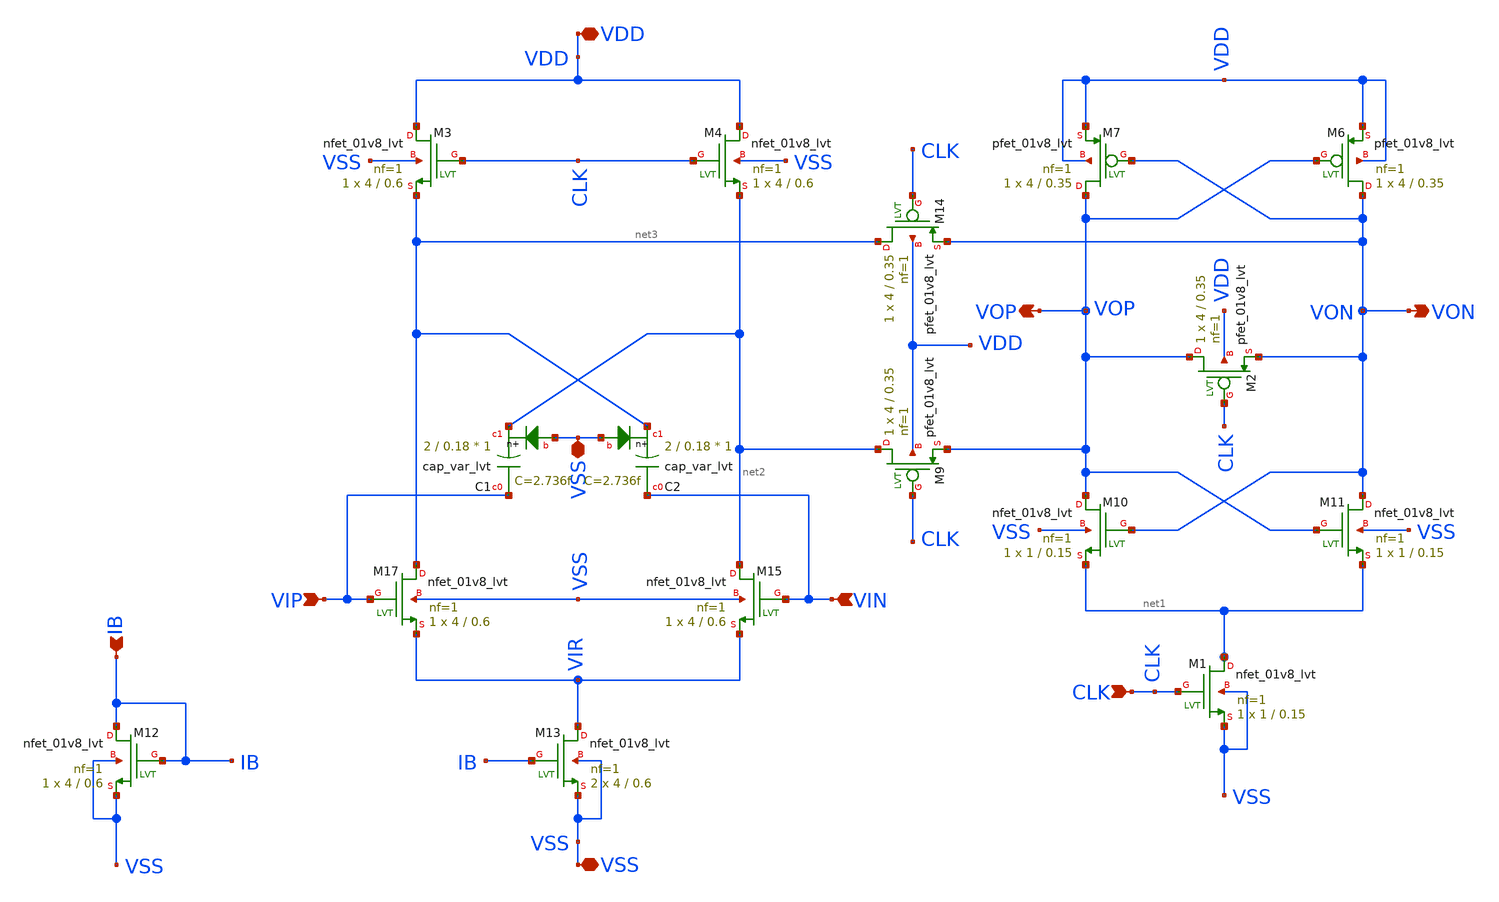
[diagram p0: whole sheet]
** sch_path: strongARM/class_AB_v3_sym.sch
**.subckt class_AB_v3_sym VDD IB VSS VIP VIN VON VOP CLK VSS
*.iopin VDD
*.ipin IB
*.iopin VSS
*.ipin VIP
*.ipin VIN
*.opin VON
*.opin VOP
*.ipin CLK
*.iopin VSS
XM17 net3 VIP VIR VSS sky130_fd_pr__nfet_01v8_lvt L=0.6 W=4 nf=1 ad='int((nf+1)/2) * W/nf * 0.29' as='int((nf+2)/2) * W/nf * 0.29'
+ pd='2*int((nf+1)/2) * (W/nf + 0.29)' ps='2*int((nf+2)/2) * (W/nf + 0.29)' nrd='0.29 / W' nrs='0.29 / W'
+ sa=0 sb=0 sd=0 mult=1 m=1
XM12 IB IB VSS VSS sky130_fd_pr__nfet_01v8_lvt L=0.6 W=4 nf=1 ad='int((nf+1)/2) * W/nf * 0.29' as='int((nf+2)/2) * W/nf * 0.29'
+ pd='2*int((nf+1)/2) * (W/nf + 0.29)' ps='2*int((nf+2)/2) * (W/nf + 0.29)' nrd='0.29 / W' nrs='0.29 / W'
+ sa=0 sb=0 sd=0 mult=1 m=1
XM15 net2 VIN VIR VSS sky130_fd_pr__nfet_01v8_lvt L=0.6 W=4 nf=1 ad='int((nf+1)/2) * W/nf * 0.29' as='int((nf+2)/2) * W/nf * 0.29'
+ pd='2*int((nf+1)/2) * (W/nf + 0.29)' ps='2*int((nf+2)/2) * (W/nf + 0.29)' nrd='0.29 / W' nrs='0.29 / W'
+ sa=0 sb=0 sd=0 mult=1 m=1
XM13 VIR IB VSS VSS sky130_fd_pr__nfet_01v8_lvt L=0.6 W=4 nf=1 ad='int((nf+1)/2) * W/nf * 0.29' as='int((nf+2)/2) * W/nf * 0.29'
+ pd='2*int((nf+1)/2) * (W/nf + 0.29)' ps='2*int((nf+2)/2) * (W/nf + 0.29)' nrd='0.29 / W' nrs='0.29 / W'
+ sa=0 sb=0 sd=0 mult=2 m=2
XM6 VON VOP VDD VDD sky130_fd_pr__pfet_01v8_lvt L=0.35 W=4 nf=1 ad='int((nf+1)/2) * W/nf * 0.29' as='int((nf+2)/2) * W/nf * 0.29'
+ pd='2*int((nf+1)/2) * (W/nf + 0.29)' ps='2*int((nf+2)/2) * (W/nf + 0.29)' nrd='0.29 / W' nrs='0.29 / W'
+ sa=0 sb=0 sd=0 mult=1 m=1
XM7 VOP VON VDD VDD sky130_fd_pr__pfet_01v8_lvt L=0.35 W=4 nf=1 ad='int((nf+1)/2) * W/nf * 0.29' as='int((nf+2)/2) * W/nf * 0.29'
+ pd='2*int((nf+1)/2) * (W/nf + 0.29)' ps='2*int((nf+2)/2) * (W/nf + 0.29)' nrd='0.29 / W' nrs='0.29 / W'
+ sa=0 sb=0 sd=0 mult=1 m=1
XM10 VOP VON net1 VSS sky130_fd_pr__nfet_01v8_lvt L=0.15 W=1 nf=1 ad='int((nf+1)/2) * W/nf * 0.29' as='int((nf+2)/2) * W/nf * 0.29'
+ pd='2*int((nf+1)/2) * (W/nf + 0.29)' ps='2*int((nf+2)/2) * (W/nf + 0.29)' nrd='0.29 / W' nrs='0.29 / W'
+ sa=0 sb=0 sd=0 mult=1 m=1
XM11 VON VOP net1 VSS sky130_fd_pr__nfet_01v8_lvt L=0.15 W=1 nf=1 ad='int((nf+1)/2) * W/nf * 0.29' as='int((nf+2)/2) * W/nf * 0.29'
+ pd='2*int((nf+1)/2) * (W/nf + 0.29)' ps='2*int((nf+2)/2) * (W/nf + 0.29)' nrd='0.29 / W' nrs='0.29 / W'
+ sa=0 sb=0 sd=0 mult=1 m=1
XM1 net1 CLK VSS VSS sky130_fd_pr__nfet_01v8_lvt L=0.15 W=1 nf=1 ad='int((nf+1)/2) * W/nf * 0.29' as='int((nf+2)/2) * W/nf * 0.29'
+ pd='2*int((nf+1)/2) * (W/nf + 0.29)' ps='2*int((nf+2)/2) * (W/nf + 0.29)' nrd='0.29 / W' nrs='0.29 / W'
+ sa=0 sb=0 sd=0 mult=1 m=1
XM2 VOP CLK VON VDD sky130_fd_pr__pfet_01v8_lvt L=0.35 W=4 nf=1 ad='int((nf+1)/2) * W/nf * 0.29' as='int((nf+2)/2) * W/nf * 0.29'
+ pd='2*int((nf+1)/2) * (W/nf + 0.29)' ps='2*int((nf+2)/2) * (W/nf + 0.29)' nrd='0.29 / W' nrs='0.29 / W'
+ sa=0 sb=0 sd=0 mult=1 m=1
XM9 net2 CLK VOP VDD sky130_fd_pr__pfet_01v8_lvt L=0.35 W=4 nf=1 ad='int((nf+1)/2) * W/nf * 0.29' as='int((nf+2)/2) * W/nf * 0.29'
+ pd='2*int((nf+1)/2) * (W/nf + 0.29)' ps='2*int((nf+2)/2) * (W/nf + 0.29)' nrd='0.29 / W' nrs='0.29 / W'
+ sa=0 sb=0 sd=0 mult=1 m=1
XM14 net3 CLK VON VDD sky130_fd_pr__pfet_01v8_lvt L=0.35 W=4 nf=1 ad='int((nf+1)/2) * W/nf * 0.29' as='int((nf+2)/2) * W/nf * 0.29'
+ pd='2*int((nf+1)/2) * (W/nf + 0.29)' ps='2*int((nf+2)/2) * (W/nf + 0.29)' nrd='0.29 / W' nrs='0.29 / W'
+ sa=0 sb=0 sd=0 mult=1 m=1
XM3 VDD CLK net3 VSS sky130_fd_pr__nfet_01v8_lvt L=0.6 W=4 nf=1 ad='int((nf+1)/2) * W/nf * 0.29' as='int((nf+2)/2) * W/nf * 0.29'
+ pd='2*int((nf+1)/2) * (W/nf + 0.29)' ps='2*int((nf+2)/2) * (W/nf + 0.29)' nrd='0.29 / W' nrs='0.29 / W'
+ sa=0 sb=0 sd=0 mult=1 m=1
XM4 VDD CLK net2 VSS sky130_fd_pr__nfet_01v8_lvt L=0.6 W=4 nf=1 ad='int((nf+1)/2) * W/nf * 0.29' as='int((nf+2)/2) * W/nf * 0.29'
+ pd='2*int((nf+1)/2) * (W/nf + 0.29)' ps='2*int((nf+2)/2) * (W/nf + 0.29)' nrd='0.29 / W' nrs='0.29 / W'
+ sa=0 sb=0 sd=0 mult=1 m=1
XC1 VIP net2 VSS sky130_fd_pr__cap_var_lvt W=2 L=0.18 VM=1 m=1
XC2 VIN net3 VSS sky130_fd_pr__cap_var_lvt W=2 L=0.18 VM=1 m=1
**.ends
.end
